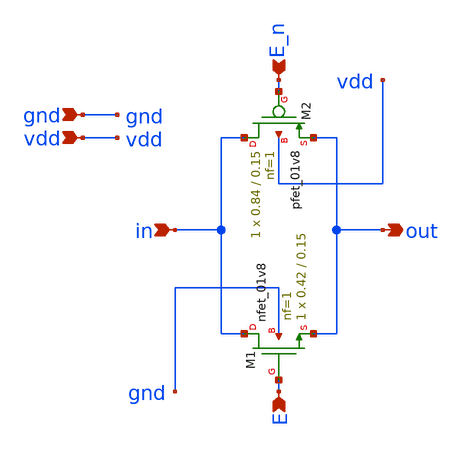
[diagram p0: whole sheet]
** sch_path: xschem/t_gate.sch
**.subckt t_gate in out E E_n vdd gnd
*.ipin in
*.opin out
*.ipin E
*.ipin E_n
*.ipin vdd
*.ipin gnd
XM1 in E out gnd sky130_fd_pr__nfet_01v8 L=0.15 W=0.42 nf=1 ad='int((nf+1)/2) * W/nf * 0.29' as='int((nf+2)/2) * W/nf * 0.29'
+ pd='2*int((nf+1)/2) * (W/nf + 0.29)' ps='2*int((nf+2)/2) * (W/nf + 0.29)' nrd='0.29 / W' nrs='0.29 / W'
+ sa=0 sb=0 sd=0 mult=1 m=1
XM2 in E_n out vdd sky130_fd_pr__pfet_01v8 L=0.15 W=0.84 nf=1 ad='int((nf+1)/2) * W/nf * 0.29' as='int((nf+2)/2) * W/nf * 0.29'
+ pd='2*int((nf+1)/2) * (W/nf + 0.29)' ps='2*int((nf+2)/2) * (W/nf + 0.29)' nrd='0.29 / W' nrs='0.29 / W'
+ sa=0 sb=0 sd=0 mult=1 m=1
**.ends
.end
